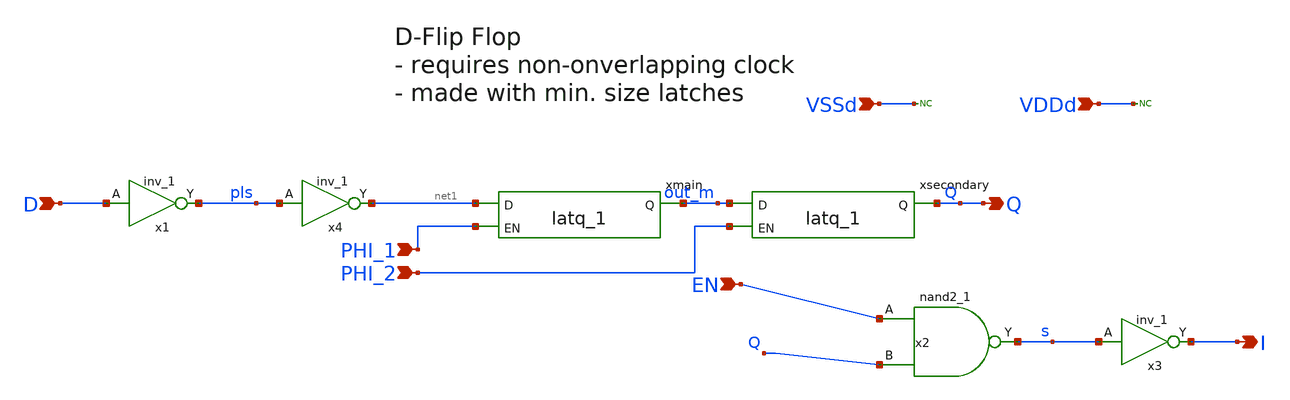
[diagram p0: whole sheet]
** sch_path: designs/libs/core_swmatrix/DFF_2phase_1.sch
**.subckt DFF_2phase_1 D PHI_1 PHI_2 Q EN I VSSd VDDd
*.ipin D
*.ipin PHI_1
*.ipin PHI_2
*.opin Q
*.ipin EN
*.opin I
*.ipin VSSd
*.ipin VDDd
xmain net1 PHI_1 out_m VDDd VDDd VSSd VSSd gf180mcu_fd_sc_mcu9t5v0__latq_1
xsecondary out_m PHI_2 Q VDDd VDDd VSSd VSSd gf180mcu_fd_sc_mcu9t5v0__latq_1
x2 EN Q VSSd VDDd VSSd VDDd s gf180mcu_fd_sc_mcu9t5v0__nand2_1
x3 s VSSd VDDd VSSd VDDd I gf180mcu_fd_sc_mcu9t5v0__inv_1
* noconn VSSd
* noconn VDDd
x1 D VSSd VDDd VSSd VDDd pls gf180mcu_fd_sc_mcu9t5v0__inv_1
x4 pls VSSd VDDd VSSd VDDd net1 gf180mcu_fd_sc_mcu9t5v0__inv_1
**.ends
.end
